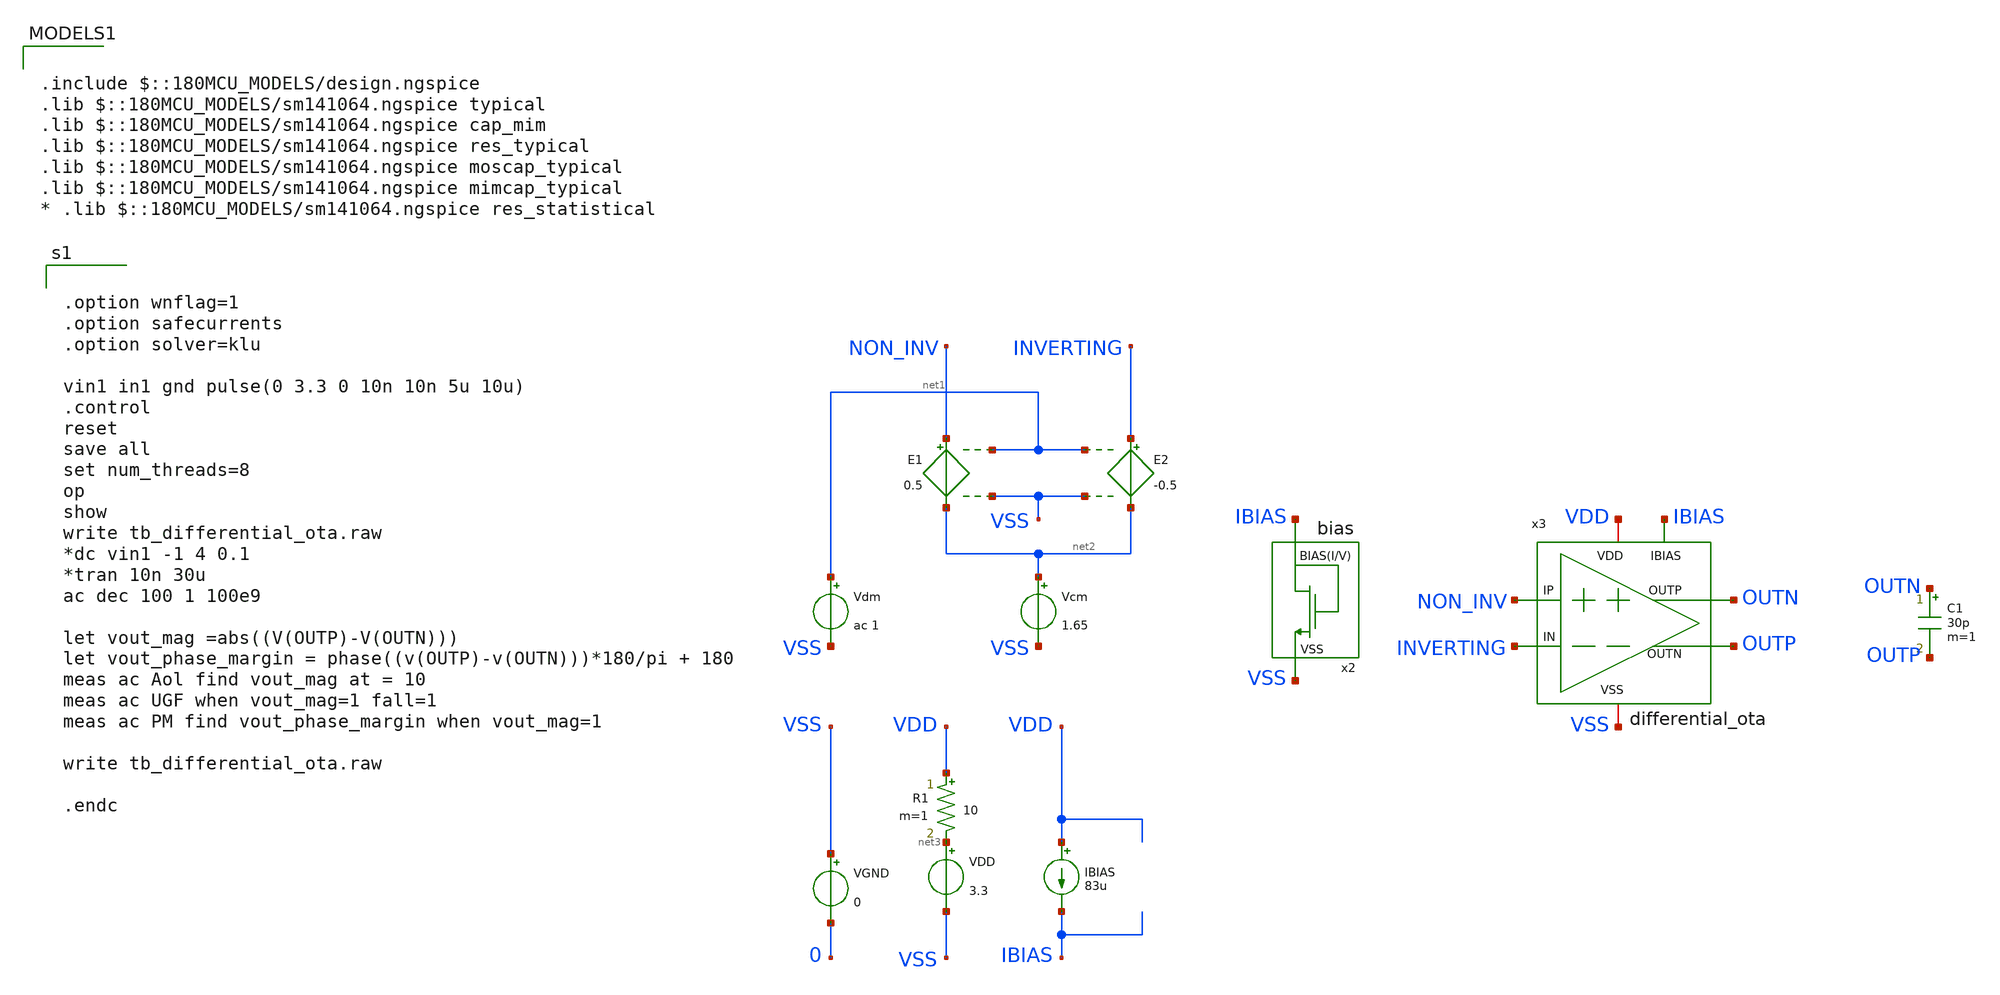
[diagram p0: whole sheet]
** sch_path: designs/libs/tb_analog/tb_differential_ota/tb_differential_ota.sch
**.subckt tb_differential_ota
E1 NON_INV net2 net1 VSS 0.5
E2 INVERTING net2 net1 VSS -0.5
Vdm net1 VSS ac 1
Vcm net2 VSS 1.65
VDD net3 VSS 3.3
R1 VDD net3 10 m=1
IBIAS VDD IBIAS 83u
VGND VSS 0 0
x2 VSS IBIAS bias
C1 OUTN OUTP 30p m=1
x3 NON_INV INVERTING IBIAS OUTN VDD VSS OUTP differential_ota
**** begin user architecture code


.option wnflag=1
.option safecurrents
.option solver=klu

vin1 in1 gnd pulse(0 3.3 0 10n 10n 5u 10u)
.control
reset
save all
set num_threads=8
op
show
write tb_differential_ota.raw
*dc vin1 -1 4 0.1
*tran 10n 30u
ac dec 100 1 100e9

let vout_mag =abs((V(OUTP)-V(OUTN)))
let vout_phase_margin = phase((v(OUTP)-v(OUTN)))*180/pi + 180
meas ac Aol find vout_mag at = 10
meas ac UGF when vout_mag=1 fall=1
meas ac PM find vout_phase_margin when vout_mag=1

write tb_differential_ota.raw

.endc



.include $::180MCU_MODELS/design.ngspice
.lib $::180MCU_MODELS/sm141064.ngspice typical
.lib $::180MCU_MODELS/sm141064.ngspice cap_mim
.lib $::180MCU_MODELS/sm141064.ngspice res_typical
.lib $::180MCU_MODELS/sm141064.ngspice moscap_typical
.lib $::180MCU_MODELS/sm141064.ngspice mimcap_typical
* .lib $::180MCU_MODELS/sm141064.ngspice res_statistical

**** end user architecture code
**.ends
.end
